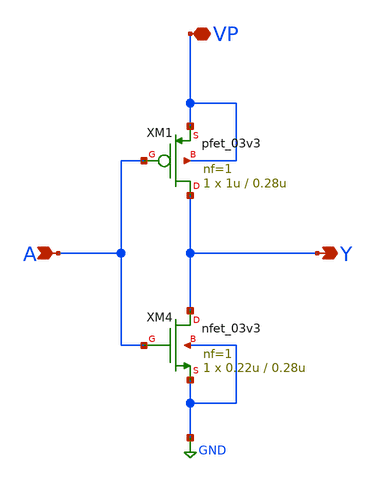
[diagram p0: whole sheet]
** sch_path: xschem/inverter.sch
**.subckt inverter A Y VP
*.ipin A
*.opin Y
*.iopin VP
XM4 Y A GND GND nfet_03v3 L=0.28u W=0.22u nf=1 ad='int((nf+1)/2) * W/nf * 0.18u' as='int((nf+2)/2) * W/nf * 0.18u'
+ pd='2*int((nf+1)/2) * (W/nf + 0.18u)' ps='2*int((nf+2)/2) * (W/nf + 0.18u)' nrd='0.18u / W' nrs='0.18u / W'
+ sa=0 sb=0 sd=0 m=1
XM1 Y A VP VP pfet_03v3 L=0.28u W=1u nf=1 ad='int((nf+1)/2) * W/nf * 0.18u' as='int((nf+2)/2) * W/nf * 0.18u'
+ pd='2*int((nf+1)/2) * (W/nf + 0.18u)' ps='2*int((nf+2)/2) * (W/nf + 0.18u)' nrd='0.18u / W' nrs='0.18u / W'
+ sa=0 sb=0 sd=0 m=1
**.ends
.GLOBAL GND
.end
